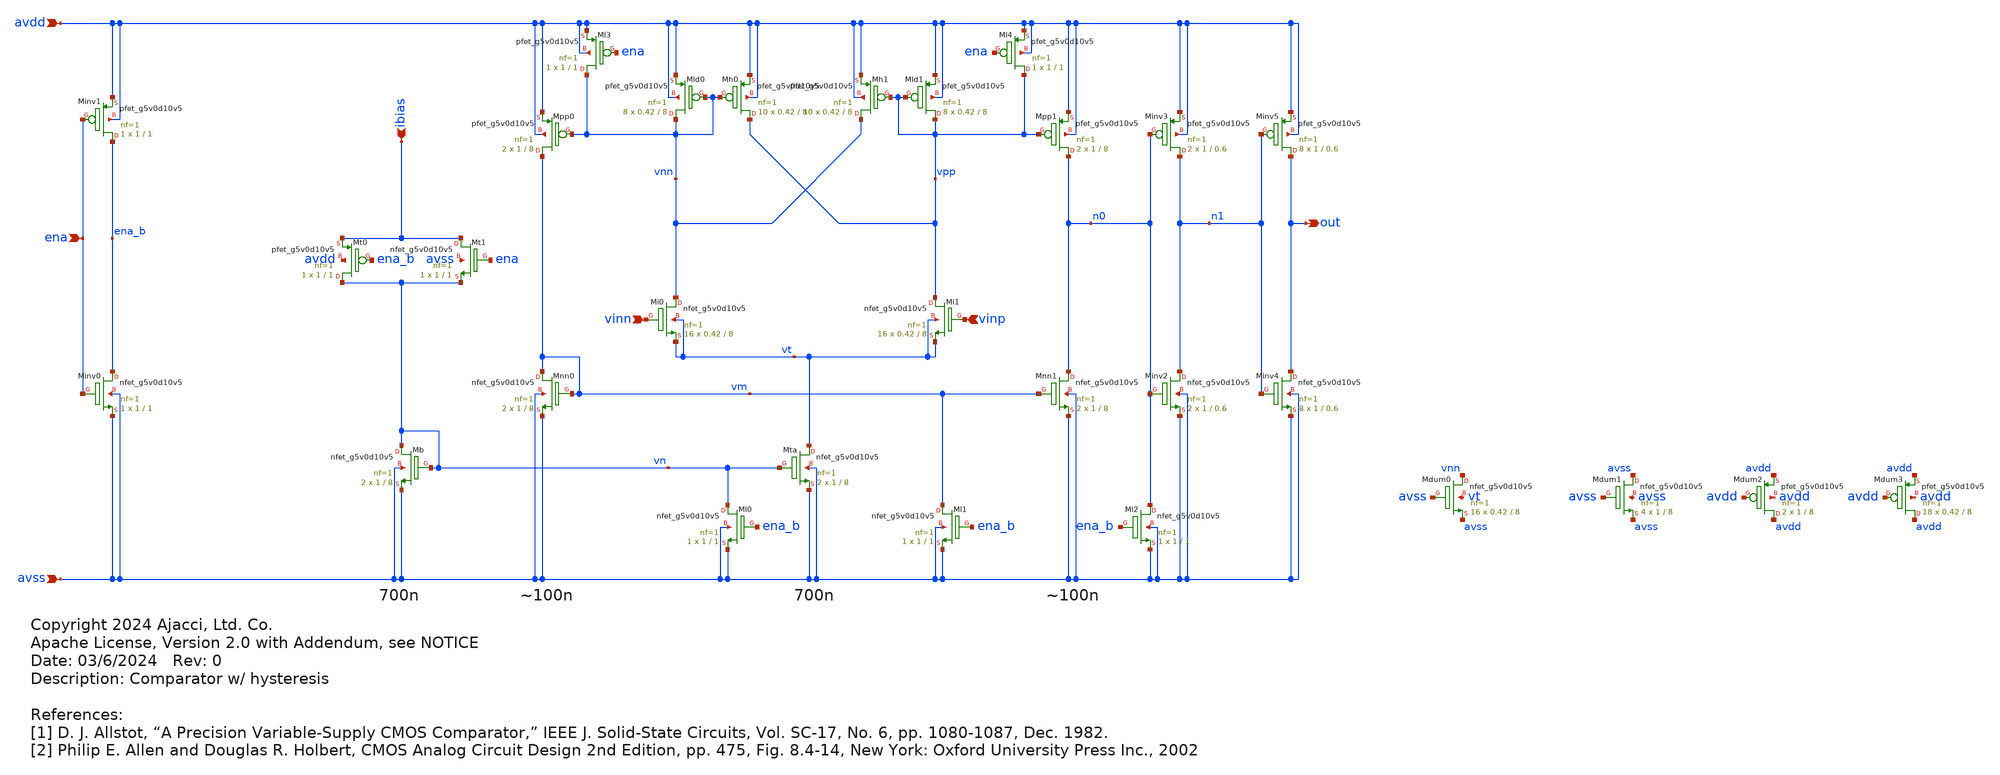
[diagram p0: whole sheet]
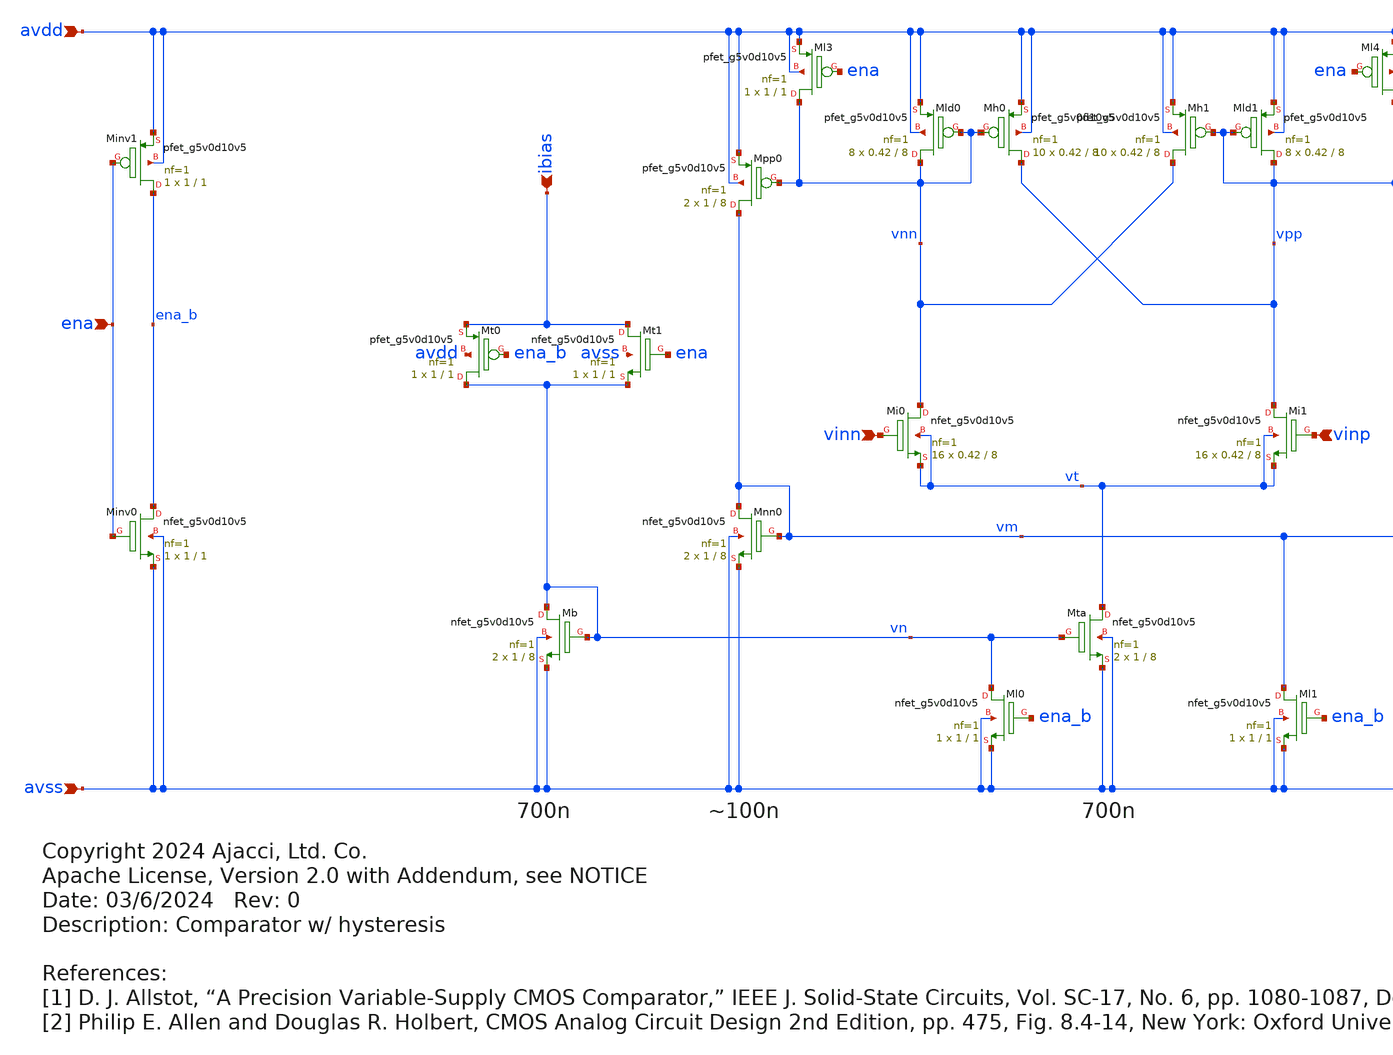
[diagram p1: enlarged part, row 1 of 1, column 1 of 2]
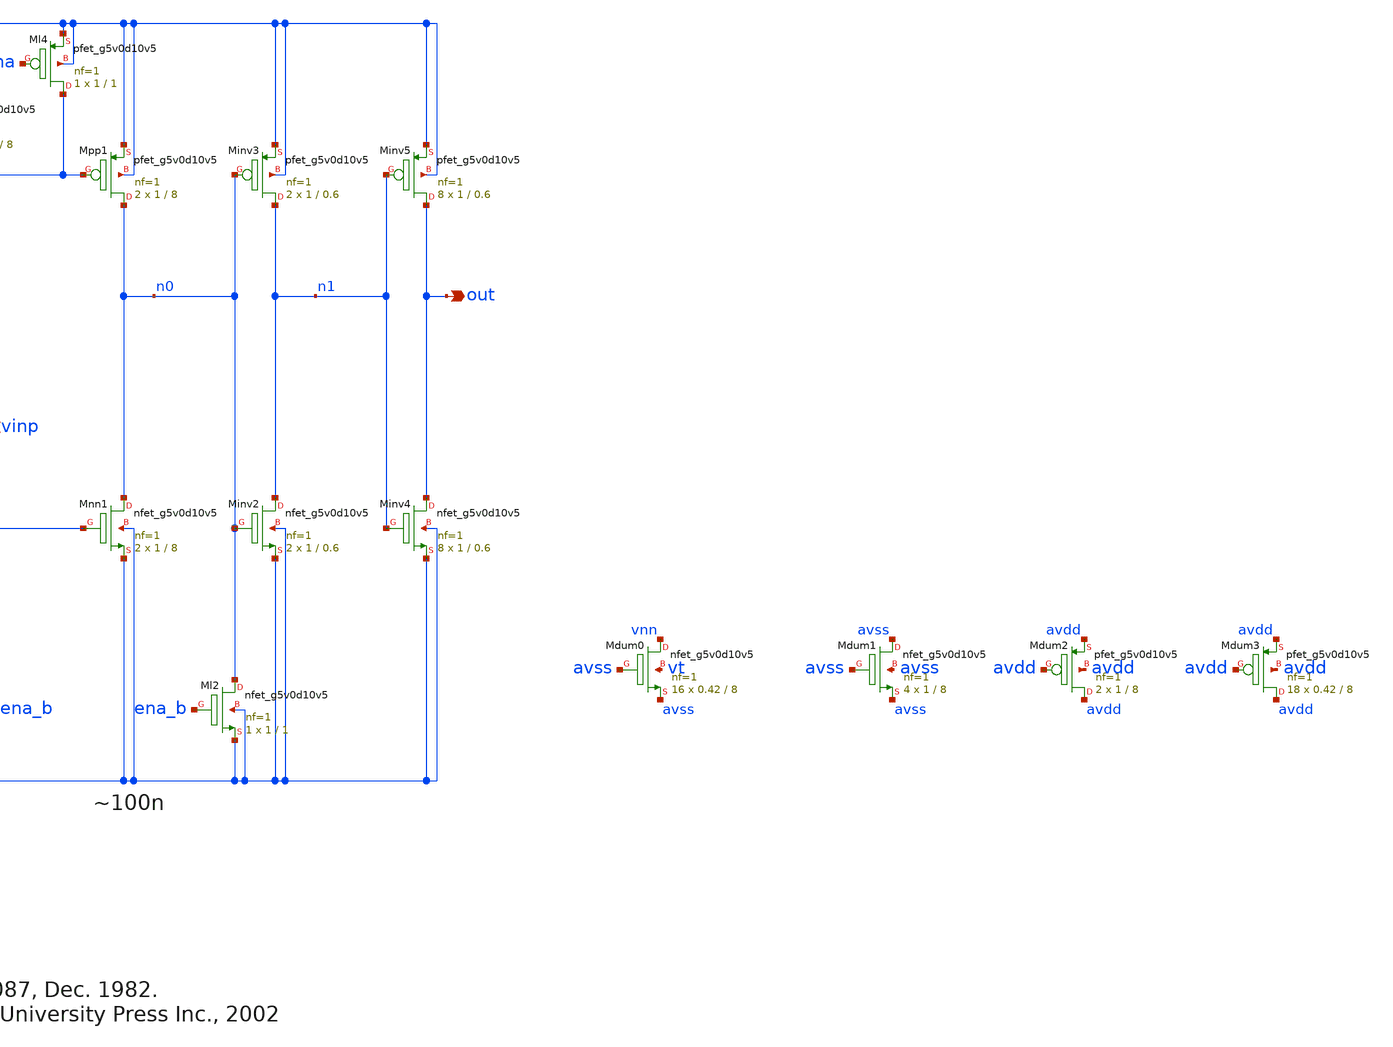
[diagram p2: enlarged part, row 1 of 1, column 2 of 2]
** sch_path: xschem/comparator.sch
* Copyright 2024 Ajacci, Ltd. Co.
* Apache License, Version 2.0 with Addendum, see NOTICE
**.subckt comparator ena avdd avss ibias vinn vinp out
*.ipin ena
*.ipin avdd
*.ipin avss
*.ipin ibias
*.ipin vinn
*.ipin vinp
*.opin out
XMb vn vn avss avss sky130_fd_pr__nfet_g5v0d10v5 L=8 W=1 nf=1 ad='int((nf+1)/2) * W/nf * 0.29' as='int((nf+2)/2) * W/nf * 0.29'
+ pd='2*int((nf+1)/2) * (W/nf + 0.29)' ps='2*int((nf+2)/2) * (W/nf + 0.29)' nrd='0.29 / W' nrs='0.29 / W'
+ sa=0 sb=0 sd=0 mult=2 m=2
XMta vt vn avss avss sky130_fd_pr__nfet_g5v0d10v5 L=8 W=1 nf=1 ad='int((nf+1)/2) * W/nf * 0.29' as='int((nf+2)/2) * W/nf * 0.29'
+ pd='2*int((nf+1)/2) * (W/nf + 0.29)' ps='2*int((nf+2)/2) * (W/nf + 0.29)' nrd='0.29 / W' nrs='0.29 / W'
+ sa=0 sb=0 sd=0 mult=2 m=2
XMl0 vn ena_b avss avss sky130_fd_pr__nfet_g5v0d10v5 L=1 W=1 nf=1 ad='int((nf+1)/2) * W/nf * 0.29' as='int((nf+2)/2) * W/nf * 0.29'
+ pd='2*int((nf+1)/2) * (W/nf + 0.29)' ps='2*int((nf+2)/2) * (W/nf + 0.29)' nrd='0.29 / W' nrs='0.29 / W'
+ sa=0 sb=0 sd=0 mult=1 m=1
XMinv0 ena_b ena avss avss sky130_fd_pr__nfet_g5v0d10v5 L=1 W=1 nf=1 ad='int((nf+1)/2) * W/nf * 0.29'
+ as='int((nf+2)/2) * W/nf * 0.29' pd='2*int((nf+1)/2) * (W/nf + 0.29)' ps='2*int((nf+2)/2) * (W/nf + 0.29)'
+ nrd='0.29 / W' nrs='0.29 / W' sa=0 sb=0 sd=0 mult=1 m=1
XMinv1 ena_b ena avdd avdd sky130_fd_pr__pfet_g5v0d10v5 L=1 W=1 nf=1 ad='int((nf+1)/2) * W/nf * 0.29'
+ as='int((nf+2)/2) * W/nf * 0.29' pd='2*int((nf+1)/2) * (W/nf + 0.29)' ps='2*int((nf+2)/2) * (W/nf + 0.29)'
+ nrd='0.29 / W' nrs='0.29 / W' sa=0 sb=0 sd=0 mult=1 m=1
XMi0 vnn vinn vt vt sky130_fd_pr__nfet_g5v0d10v5 L=8 W=0.42 nf=1 ad='int((nf+1)/2) * W/nf * 0.29' as='int((nf+2)/2) * W/nf * 0.29'
+ pd='2*int((nf+1)/2) * (W/nf + 0.29)' ps='2*int((nf+2)/2) * (W/nf + 0.29)' nrd='0.29 / W' nrs='0.29 / W'
+ sa=0 sb=0 sd=0 mult=16 m=16
XMi1 vpp vinp vt vt sky130_fd_pr__nfet_g5v0d10v5 L=8 W=0.42 nf=1 ad='int((nf+1)/2) * W/nf * 0.29' as='int((nf+2)/2) * W/nf * 0.29'
+ pd='2*int((nf+1)/2) * (W/nf + 0.29)' ps='2*int((nf+2)/2) * (W/nf + 0.29)' nrd='0.29 / W' nrs='0.29 / W'
+ sa=0 sb=0 sd=0 mult=16 m=16
XMld1 vpp vpp avdd avdd sky130_fd_pr__pfet_g5v0d10v5 L=8 W=0.42 nf=1 ad='int((nf+1)/2) * W/nf * 0.29'
+ as='int((nf+2)/2) * W/nf * 0.29' pd='2*int((nf+1)/2) * (W/nf + 0.29)' ps='2*int((nf+2)/2) * (W/nf + 0.29)'
+ nrd='0.29 / W' nrs='0.29 / W' sa=0 sb=0 sd=0 mult=8 m=8
XMh1 vnn vpp avdd avdd sky130_fd_pr__pfet_g5v0d10v5 L=8 W=0.42 nf=1 ad='int((nf+1)/2) * W/nf * 0.29'
+ as='int((nf+2)/2) * W/nf * 0.29' pd='2*int((nf+1)/2) * (W/nf + 0.29)' ps='2*int((nf+2)/2) * (W/nf + 0.29)'
+ nrd='0.29 / W' nrs='0.29 / W' sa=0 sb=0 sd=0 mult=10 m=10
XMh0 vpp vnn avdd avdd sky130_fd_pr__pfet_g5v0d10v5 L=8 W=0.42 nf=1 ad='int((nf+1)/2) * W/nf * 0.29'
+ as='int((nf+2)/2) * W/nf * 0.29' pd='2*int((nf+1)/2) * (W/nf + 0.29)' ps='2*int((nf+2)/2) * (W/nf + 0.29)'
+ nrd='0.29 / W' nrs='0.29 / W' sa=0 sb=0 sd=0 mult=10 m=10
XMld0 vnn vnn avdd avdd sky130_fd_pr__pfet_g5v0d10v5 L=8 W=0.42 nf=1 ad='int((nf+1)/2) * W/nf * 0.29'
+ as='int((nf+2)/2) * W/nf * 0.29' pd='2*int((nf+1)/2) * (W/nf + 0.29)' ps='2*int((nf+2)/2) * (W/nf + 0.29)'
+ nrd='0.29 / W' nrs='0.29 / W' sa=0 sb=0 sd=0 mult=8 m=8
XMpp1 n0 vpp avdd avdd sky130_fd_pr__pfet_g5v0d10v5 L=8 W=1 nf=1 ad='int((nf+1)/2) * W/nf * 0.29' as='int((nf+2)/2) * W/nf * 0.29'
+ pd='2*int((nf+1)/2) * (W/nf + 0.29)' ps='2*int((nf+2)/2) * (W/nf + 0.29)' nrd='0.29 / W' nrs='0.29 / W'
+ sa=0 sb=0 sd=0 mult=2 m=2
XMnn1 n0 vm avss avss sky130_fd_pr__nfet_g5v0d10v5 L=8 W=1 nf=1 ad='int((nf+1)/2) * W/nf * 0.29' as='int((nf+2)/2) * W/nf * 0.29'
+ pd='2*int((nf+1)/2) * (W/nf + 0.29)' ps='2*int((nf+2)/2) * (W/nf + 0.29)' nrd='0.29 / W' nrs='0.29 / W'
+ sa=0 sb=0 sd=0 mult=2 m=2
XMpp0 vm vnn avdd avdd sky130_fd_pr__pfet_g5v0d10v5 L=8 W=1 nf=1 ad='int((nf+1)/2) * W/nf * 0.29' as='int((nf+2)/2) * W/nf * 0.29'
+ pd='2*int((nf+1)/2) * (W/nf + 0.29)' ps='2*int((nf+2)/2) * (W/nf + 0.29)' nrd='0.29 / W' nrs='0.29 / W'
+ sa=0 sb=0 sd=0 mult=2 m=2
XMnn0 vm vm avss avss sky130_fd_pr__nfet_g5v0d10v5 L=8 W=1 nf=1 ad='int((nf+1)/2) * W/nf * 0.29' as='int((nf+2)/2) * W/nf * 0.29'
+ pd='2*int((nf+1)/2) * (W/nf + 0.29)' ps='2*int((nf+2)/2) * (W/nf + 0.29)' nrd='0.29 / W' nrs='0.29 / W'
+ sa=0 sb=0 sd=0 mult=2 m=2
XMinv3 n1 n0 avdd avdd sky130_fd_pr__pfet_g5v0d10v5 L=0.6 W=1 nf=1 ad='int((nf+1)/2) * W/nf * 0.29' as='int((nf+2)/2) * W/nf * 0.29'
+ pd='2*int((nf+1)/2) * (W/nf + 0.29)' ps='2*int((nf+2)/2) * (W/nf + 0.29)' nrd='0.29 / W' nrs='0.29 / W'
+ sa=0 sb=0 sd=0 mult=2 m=2
XMinv2 n1 n0 avss avss sky130_fd_pr__nfet_g5v0d10v5 L=0.6 W=1 nf=1 ad='int((nf+1)/2) * W/nf * 0.29' as='int((nf+2)/2) * W/nf * 0.29'
+ pd='2*int((nf+1)/2) * (W/nf + 0.29)' ps='2*int((nf+2)/2) * (W/nf + 0.29)' nrd='0.29 / W' nrs='0.29 / W'
+ sa=0 sb=0 sd=0 mult=2 m=2
XMinv5 out n1 avdd avdd sky130_fd_pr__pfet_g5v0d10v5 L=0.6 W=1 nf=1 ad='int((nf+1)/2) * W/nf * 0.29'
+ as='int((nf+2)/2) * W/nf * 0.29' pd='2*int((nf+1)/2) * (W/nf + 0.29)' ps='2*int((nf+2)/2) * (W/nf + 0.29)'
+ nrd='0.29 / W' nrs='0.29 / W' sa=0 sb=0 sd=0 mult=8 m=8
XMinv4 out n1 avss avss sky130_fd_pr__nfet_g5v0d10v5 L=0.6 W=1 nf=1 ad='int((nf+1)/2) * W/nf * 0.29'
+ as='int((nf+2)/2) * W/nf * 0.29' pd='2*int((nf+1)/2) * (W/nf + 0.29)' ps='2*int((nf+2)/2) * (W/nf + 0.29)'
+ nrd='0.29 / W' nrs='0.29 / W' sa=0 sb=0 sd=0 mult=8 m=8
XMl1 vm ena_b avss avss sky130_fd_pr__nfet_g5v0d10v5 L=1 W=1 nf=1 ad='int((nf+1)/2) * W/nf * 0.29' as='int((nf+2)/2) * W/nf * 0.29'
+ pd='2*int((nf+1)/2) * (W/nf + 0.29)' ps='2*int((nf+2)/2) * (W/nf + 0.29)' nrd='0.29 / W' nrs='0.29 / W'
+ sa=0 sb=0 sd=0 mult=1 m=1
XMl3 vnn ena avdd avdd sky130_fd_pr__pfet_g5v0d10v5 L=1 W=1 nf=1 ad='int((nf+1)/2) * W/nf * 0.29' as='int((nf+2)/2) * W/nf * 0.29'
+ pd='2*int((nf+1)/2) * (W/nf + 0.29)' ps='2*int((nf+2)/2) * (W/nf + 0.29)' nrd='0.29 / W' nrs='0.29 / W'
+ sa=0 sb=0 sd=0 mult=1 m=1
XMl4 vpp ena avdd avdd sky130_fd_pr__pfet_g5v0d10v5 L=1 W=1 nf=1 ad='int((nf+1)/2) * W/nf * 0.29' as='int((nf+2)/2) * W/nf * 0.29'
+ pd='2*int((nf+1)/2) * (W/nf + 0.29)' ps='2*int((nf+2)/2) * (W/nf + 0.29)' nrd='0.29 / W' nrs='0.29 / W'
+ sa=0 sb=0 sd=0 mult=1 m=1
XMt1 ibias ena vn avss sky130_fd_pr__nfet_g5v0d10v5 L=1 W=1 nf=1 ad='int((nf+1)/2) * W/nf * 0.29' as='int((nf+2)/2) * W/nf * 0.29'
+ pd='2*int((nf+1)/2) * (W/nf + 0.29)' ps='2*int((nf+2)/2) * (W/nf + 0.29)' nrd='0.29 / W' nrs='0.29 / W'
+ sa=0 sb=0 sd=0 mult=1 m=1
XMt0 vn ena_b ibias avdd sky130_fd_pr__pfet_g5v0d10v5 L=1 W=1 nf=1 ad='int((nf+1)/2) * W/nf * 0.29' as='int((nf+2)/2) * W/nf * 0.29'
+ pd='2*int((nf+1)/2) * (W/nf + 0.29)' ps='2*int((nf+2)/2) * (W/nf + 0.29)' nrd='0.29 / W' nrs='0.29 / W'
+ sa=0 sb=0 sd=0 mult=1 m=1
XMl2 n0 ena_b avss avss sky130_fd_pr__nfet_g5v0d10v5 L=1 W=1 nf=1 ad='int((nf+1)/2) * W/nf * 0.29' as='int((nf+2)/2) * W/nf * 0.29'
+ pd='2*int((nf+1)/2) * (W/nf + 0.29)' ps='2*int((nf+2)/2) * (W/nf + 0.29)' nrd='0.29 / W' nrs='0.29 / W'
+ sa=0 sb=0 sd=0 mult=1 m=1
XMdum0 vnn avss avss vt sky130_fd_pr__nfet_g5v0d10v5 L=8 W=0.42 nf=1 ad='int((nf+1)/2) * W/nf * 0.29'
+ as='int((nf+2)/2) * W/nf * 0.29' pd='2*int((nf+1)/2) * (W/nf + 0.29)' ps='2*int((nf+2)/2) * (W/nf + 0.29)'
+ nrd='0.29 / W' nrs='0.29 / W' sa=0 sb=0 sd=0 mult=16 m=16
XMdum1 avss avss avss avss sky130_fd_pr__nfet_g5v0d10v5 L=8 W=1 nf=1 ad='int((nf+1)/2) * W/nf * 0.29'
+ as='int((nf+2)/2) * W/nf * 0.29' pd='2*int((nf+1)/2) * (W/nf + 0.29)' ps='2*int((nf+2)/2) * (W/nf + 0.29)'
+ nrd='0.29 / W' nrs='0.29 / W' sa=0 sb=0 sd=0 mult=4 m=4
XMdum2 avdd avdd avdd avdd sky130_fd_pr__pfet_g5v0d10v5 L=8 W=1 nf=1 ad='int((nf+1)/2) * W/nf * 0.29'
+ as='int((nf+2)/2) * W/nf * 0.29' pd='2*int((nf+1)/2) * (W/nf + 0.29)' ps='2*int((nf+2)/2) * (W/nf + 0.29)'
+ nrd='0.29 / W' nrs='0.29 / W' sa=0 sb=0 sd=0 mult=2 m=2
XMdum3 avdd avdd avdd avdd sky130_fd_pr__pfet_g5v0d10v5 L=8 W=0.42 nf=1 ad='int((nf+1)/2) * W/nf * 0.29'
+ as='int((nf+2)/2) * W/nf * 0.29' pd='2*int((nf+1)/2) * (W/nf + 0.29)' ps='2*int((nf+2)/2) * (W/nf + 0.29)'
+ nrd='0.29 / W' nrs='0.29 / W' sa=0 sb=0 sd=0 mult=18 m=18
**.ends
.end
